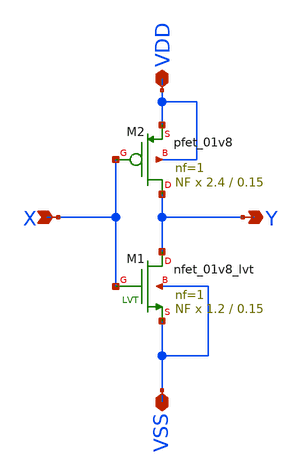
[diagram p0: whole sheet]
** sch_path: xschem_lib/DFFRAM_full_custom/inv.sch
**.subckt inv VSS X Y VDD
*.iopin VSS
*.ipin X
*.opin Y
*.iopin VDD
XM1 Y X VSS VSS sky130_fd_pr__nfet_01v8_lvt L=0.15 W=1.2 nf=1 ad='int((nf+1)/2) * W/nf * 0.29' as='int((nf+2)/2) * W/nf * 0.29'
+ pd='2*int((nf+1)/2) * (W/nf + 0.29)' ps='2*int((nf+2)/2) * (W/nf + 0.29)' nrd='0.29 / W' nrs='0.29 / W'
+ sa=0 sb=0 sd=0 mult=NF m=NF
XM2 Y X VDD VDD sky130_fd_pr__pfet_01v8 L=0.15 W=2.4 nf=1 ad='int((nf+1)/2) * W/nf * 0.29' as='int((nf+2)/2) * W/nf * 0.29'
+ pd='2*int((nf+1)/2) * (W/nf + 0.29)' ps='2*int((nf+2)/2) * (W/nf + 0.29)' nrd='0.29 / W' nrs='0.29 / W'
+ sa=0 sb=0 sd=0 mult=NF m=NF
**.ends
.end
